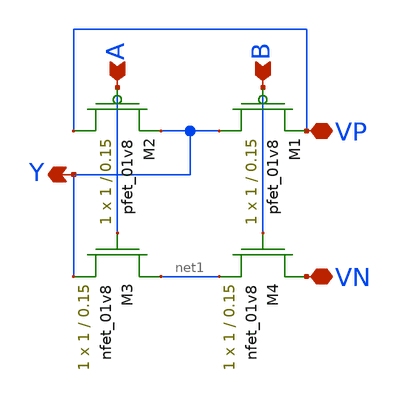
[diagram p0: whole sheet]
** sch_path: Miniproject1/NAND_LDS.sch
**.subckt NAND_LDS Y A B VP VN
*.opin Y
*.ipin A
*.ipin B
*.iopin VP
*.iopin VN
XM1 Y B VP VDD sky130_fd_pr__pfet_01v8 L=0.15 W=1 nf=1 ad='int((nf+1)/2) * W/nf * 0.29' as='int((nf+2)/2) * W/nf * 0.29'
+ pd='2*int((nf+1)/2) * (W/nf + 0.29)' ps='2*int((nf+2)/2) * (W/nf + 0.29)' nrd='0.29 / W' nrs='0.29 / W'
+ sa=0 sb=0 sd=0 mult=1 m=1
XM2 VP A Y VDD sky130_fd_pr__pfet_01v8 L=0.15 W=1 nf=1 ad='int((nf+1)/2) * W/nf * 0.29' as='int((nf+2)/2) * W/nf * 0.29'
+ pd='2*int((nf+1)/2) * (W/nf + 0.29)' ps='2*int((nf+2)/2) * (W/nf + 0.29)' nrd='0.29 / W' nrs='0.29 / W'
+ sa=0 sb=0 sd=0 mult=1 m=1
XM3 net1 A Y GND sky130_fd_pr__nfet_01v8 L=0.15 W=1 nf=1 ad='int((nf+1)/2) * W/nf * 0.29' as='int((nf+2)/2) * W/nf * 0.29'
+ pd='2*int((nf+1)/2) * (W/nf + 0.29)' ps='2*int((nf+2)/2) * (W/nf + 0.29)' nrd='0.29 / W' nrs='0.29 / W'
+ sa=0 sb=0 sd=0 mult=1 m=1
XM4 VN B net1 GND sky130_fd_pr__nfet_01v8 L=0.15 W=1 nf=1 ad='int((nf+1)/2) * W/nf * 0.29' as='int((nf+2)/2) * W/nf * 0.29'
+ pd='2*int((nf+1)/2) * (W/nf + 0.29)' ps='2*int((nf+2)/2) * (W/nf + 0.29)' nrd='0.29 / W' nrs='0.29 / W'
+ sa=0 sb=0 sd=0 mult=1 m=1
**.ends
.end
